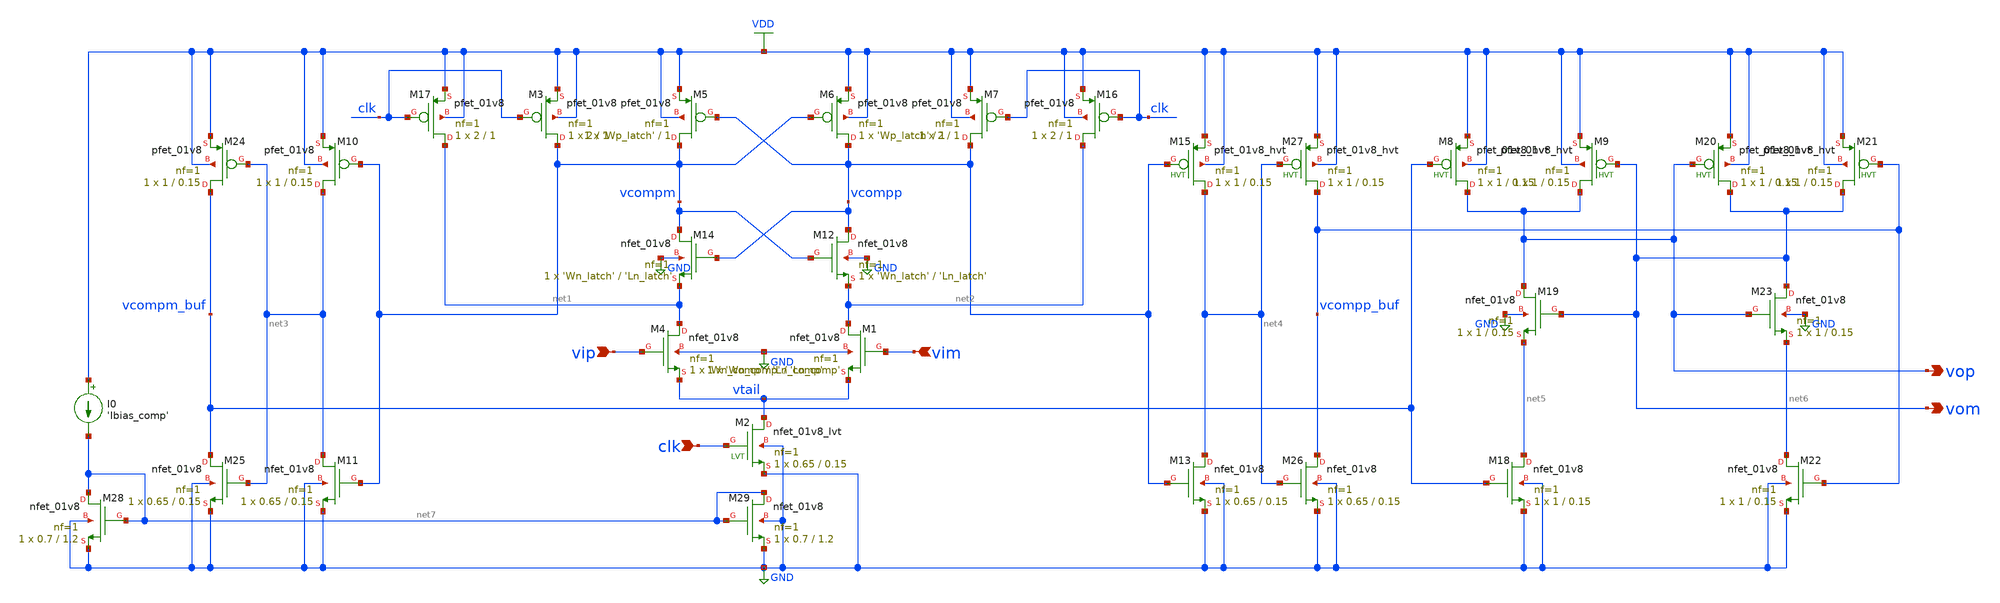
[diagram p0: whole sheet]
** sch_path: designs/latched_comparator.sch
* Copyright 2020 Stefan Frederik Schippers
* Licensed under the Apache License, Version 2.0 (the "License");
* you may not use this file except in compliance with the License.
* You may obtain a copy of the License at
* https://www.apache.org/licenses/LICENSE-2.0
* Unless required by applicable law or agreed to in writing, software
* distributed under the License is distributed on an "AS IS" BASIS,
* WITHOUT WARRANTIES OR CONDITIONS OF ANY KIND, either express or implied.
* See the License for the specific language governing permissions and
* limitations under the License.
**.subckt latched_comparator vip vim vop clk vom
*.ipin vip
*.ipin vim
*.opin vop
*.ipin clk
*.opin vom
XM5 vcompm vcompp VDD VDD sky130_fd_pr__pfet_01v8 L=1 W='Wp_latch' nf=1 ad='int((nf+1)/2) * W/nf * 0.29'
+ as='int((nf+2)/2) * W/nf * 0.29' pd='2*int((nf+1)/2) * (W/nf + 0.29)' ps='2*int((nf+2)/2) * (W/nf + 0.29)'
+ nrd='0.29 / W' nrs='0.29 / W' sa=0 sb=0 sd=0 mult=1 m=1
XM10 net3 vcompm VDD VDD sky130_fd_pr__pfet_01v8 L=0.15 W=1 nf=1 ad='int((nf+1)/2) * W/nf * 0.29' as='int((nf+2)/2) * W/nf * 0.29'
+ pd='2*int((nf+1)/2) * (W/nf + 0.29)' ps='2*int((nf+2)/2) * (W/nf + 0.29)' nrd='0.29 / W' nrs='0.29 / W'
+ sa=0 sb=0 sd=0 mult=1 m=1
XM11 net3 vcompm GND GND sky130_fd_pr__nfet_01v8 L=0.15 W=0.65 nf=1 ad='int((nf+1)/2) * W/nf * 0.29'
+ as='int((nf+2)/2) * W/nf * 0.29' pd='2*int((nf+1)/2) * (W/nf + 0.29)' ps='2*int((nf+2)/2) * (W/nf + 0.29)'
+ nrd='0.29 / W' nrs='0.29 / W' sa=0 sb=0 sd=0 mult=1 m=1
XM13 net4 vcompp GND GND sky130_fd_pr__nfet_01v8 L=0.15 W=0.65 nf=1 ad='int((nf+1)/2) * W/nf * 0.29'
+ as='int((nf+2)/2) * W/nf * 0.29' pd='2*int((nf+1)/2) * (W/nf + 0.29)' ps='2*int((nf+2)/2) * (W/nf + 0.29)'
+ nrd='0.29 / W' nrs='0.29 / W' sa=0 sb=0 sd=0 mult=1 m=1
XM15 net4 vcompp VDD VDD sky130_fd_pr__pfet_01v8_hvt L=0.15 W=1 nf=1 ad='int((nf+1)/2) * W/nf * 0.29'
+ as='int((nf+2)/2) * W/nf * 0.29' pd='2*int((nf+1)/2) * (W/nf + 0.29)' ps='2*int((nf+2)/2) * (W/nf + 0.29)'
+ nrd='0.29 / W' nrs='0.29 / W' sa=0 sb=0 sd=0 mult=1 m=1
XM6 vcompp vcompm VDD VDD sky130_fd_pr__pfet_01v8 L=1 W='Wp_latch' nf=1 ad='int((nf+1)/2) * W/nf * 0.29'
+ as='int((nf+2)/2) * W/nf * 0.29' pd='2*int((nf+1)/2) * (W/nf + 0.29)' ps='2*int((nf+2)/2) * (W/nf + 0.29)'
+ nrd='0.29 / W' nrs='0.29 / W' sa=0 sb=0 sd=0 mult=1 m=1
XM12 vcompp vcompm net2 GND sky130_fd_pr__nfet_01v8 L='Ln_latch' W='Wn_latch' nf=1 ad='int((nf+1)/2) * W/nf * 0.29'
+ as='int((nf+2)/2) * W/nf * 0.29' pd='2*int((nf+1)/2) * (W/nf + 0.29)' ps='2*int((nf+2)/2) * (W/nf + 0.29)'
+ nrd='0.29 / W' nrs='0.29 / W' sa=0 sb=0 sd=0 mult=1 m=1
XM14 vcompm vcompp net1 GND sky130_fd_pr__nfet_01v8 L='Ln_latch' W='Wn_latch' nf=1 ad='int((nf+1)/2) * W/nf * 0.29'
+ as='int((nf+2)/2) * W/nf * 0.29' pd='2*int((nf+1)/2) * (W/nf + 0.29)' ps='2*int((nf+2)/2) * (W/nf + 0.29)'
+ nrd='0.29 / W' nrs='0.29 / W' sa=0 sb=0 sd=0 mult=1 m=1
XM3 vcompm clk VDD VDD sky130_fd_pr__pfet_01v8 L=1 W=2 nf=1 ad='int((nf+1)/2) * W/nf * 0.29' as='int((nf+2)/2) * W/nf * 0.29'
+ pd='2*int((nf+1)/2) * (W/nf + 0.29)' ps='2*int((nf+2)/2) * (W/nf + 0.29)' nrd='0.29 / W' nrs='0.29 / W'
+ sa=0 sb=0 sd=0 mult=1 m=1
XM7 vcompp clk VDD VDD sky130_fd_pr__pfet_01v8 L=1 W=2 nf=1 ad='int((nf+1)/2) * W/nf * 0.29' as='int((nf+2)/2) * W/nf * 0.29'
+ pd='2*int((nf+1)/2) * (W/nf + 0.29)' ps='2*int((nf+2)/2) * (W/nf + 0.29)' nrd='0.29 / W' nrs='0.29 / W'
+ sa=0 sb=0 sd=0 mult=1 m=1
XM16 net2 clk VDD VDD sky130_fd_pr__pfet_01v8 L=1 W=2 nf=1 ad='int((nf+1)/2) * W/nf * 0.29' as='int((nf+2)/2) * W/nf * 0.29'
+ pd='2*int((nf+1)/2) * (W/nf + 0.29)' ps='2*int((nf+2)/2) * (W/nf + 0.29)' nrd='0.29 / W' nrs='0.29 / W'
+ sa=0 sb=0 sd=0 mult=1 m=1
XM17 net1 clk VDD VDD sky130_fd_pr__pfet_01v8 L=1 W=2 nf=1 ad='int((nf+1)/2) * W/nf * 0.29' as='int((nf+2)/2) * W/nf * 0.29'
+ pd='2*int((nf+1)/2) * (W/nf + 0.29)' ps='2*int((nf+2)/2) * (W/nf + 0.29)' nrd='0.29 / W' nrs='0.29 / W'
+ sa=0 sb=0 sd=0 mult=1 m=1
XM8 vop vcompm_buf VDD VDD sky130_fd_pr__pfet_01v8_hvt L=0.15 W=1 nf=1 ad='int((nf+1)/2) * W/nf * 0.29'
+ as='int((nf+2)/2) * W/nf * 0.29' pd='2*int((nf+1)/2) * (W/nf + 0.29)' ps='2*int((nf+2)/2) * (W/nf + 0.29)'
+ nrd='0.29 / W' nrs='0.29 / W' sa=0 sb=0 sd=0 mult=1 m=1
XM9 vop vom VDD VDD sky130_fd_pr__pfet_01v8_hvt L=0.15 W=1 nf=1 ad='int((nf+1)/2) * W/nf * 0.29' as='int((nf+2)/2) * W/nf * 0.29'
+ pd='2*int((nf+1)/2) * (W/nf + 0.29)' ps='2*int((nf+2)/2) * (W/nf + 0.29)' nrd='0.29 / W' nrs='0.29 / W'
+ sa=0 sb=0 sd=0 mult=1 m=1
XM18 net5 vcompm_buf GND GND sky130_fd_pr__nfet_01v8 L=0.15 W=1 nf=1 ad='int((nf+1)/2) * W/nf * 0.29'
+ as='int((nf+2)/2) * W/nf * 0.29' pd='2*int((nf+1)/2) * (W/nf + 0.29)' ps='2*int((nf+2)/2) * (W/nf + 0.29)'
+ nrd='0.29 / W' nrs='0.29 / W' sa=0 sb=0 sd=0 mult=1 m=1
XM19 vop vom net5 GND sky130_fd_pr__nfet_01v8 L=0.15 W=1 nf=1 ad='int((nf+1)/2) * W/nf * 0.29' as='int((nf+2)/2) * W/nf * 0.29'
+ pd='2*int((nf+1)/2) * (W/nf + 0.29)' ps='2*int((nf+2)/2) * (W/nf + 0.29)' nrd='0.29 / W' nrs='0.29 / W'
+ sa=0 sb=0 sd=0 mult=1 m=1
XM20 vom vop VDD VDD sky130_fd_pr__pfet_01v8_hvt L=0.15 W=1 nf=1 ad='int((nf+1)/2) * W/nf * 0.29' as='int((nf+2)/2) * W/nf * 0.29'
+ pd='2*int((nf+1)/2) * (W/nf + 0.29)' ps='2*int((nf+2)/2) * (W/nf + 0.29)' nrd='0.29 / W' nrs='0.29 / W'
+ sa=0 sb=0 sd=0 mult=1 m=1
XM21 vom vcompp_buf VDD VDD sky130_fd_pr__pfet_01v8_hvt L=0.15 W=1 nf=1 ad='int((nf+1)/2) * W/nf * 0.29'
+ as='int((nf+2)/2) * W/nf * 0.29' pd='2*int((nf+1)/2) * (W/nf + 0.29)' ps='2*int((nf+2)/2) * (W/nf + 0.29)'
+ nrd='0.29 / W' nrs='0.29 / W' sa=0 sb=0 sd=0 mult=1 m=1
XM22 net6 vcompp_buf GND GND sky130_fd_pr__nfet_01v8 L=0.15 W=1 nf=1 ad='int((nf+1)/2) * W/nf * 0.29'
+ as='int((nf+2)/2) * W/nf * 0.29' pd='2*int((nf+1)/2) * (W/nf + 0.29)' ps='2*int((nf+2)/2) * (W/nf + 0.29)'
+ nrd='0.29 / W' nrs='0.29 / W' sa=0 sb=0 sd=0 mult=1 m=1
XM23 vom vop net6 GND sky130_fd_pr__nfet_01v8 L=0.15 W=1 nf=1 ad='int((nf+1)/2) * W/nf * 0.29' as='int((nf+2)/2) * W/nf * 0.29'
+ pd='2*int((nf+1)/2) * (W/nf + 0.29)' ps='2*int((nf+2)/2) * (W/nf + 0.29)' nrd='0.29 / W' nrs='0.29 / W'
+ sa=0 sb=0 sd=0 mult=1 m=1
XM24 vcompm_buf net3 VDD VDD sky130_fd_pr__pfet_01v8 L=0.15 W=1 nf=1 ad='int((nf+1)/2) * W/nf * 0.29'
+ as='int((nf+2)/2) * W/nf * 0.29' pd='2*int((nf+1)/2) * (W/nf + 0.29)' ps='2*int((nf+2)/2) * (W/nf + 0.29)'
+ nrd='0.29 / W' nrs='0.29 / W' sa=0 sb=0 sd=0 mult=1 m=1
XM25 vcompm_buf net3 GND GND sky130_fd_pr__nfet_01v8 L=0.15 W=0.65 nf=1 ad='int((nf+1)/2) * W/nf * 0.29'
+ as='int((nf+2)/2) * W/nf * 0.29' pd='2*int((nf+1)/2) * (W/nf + 0.29)' ps='2*int((nf+2)/2) * (W/nf + 0.29)'
+ nrd='0.29 / W' nrs='0.29 / W' sa=0 sb=0 sd=0 mult=1 m=1
XM26 vcompp_buf net4 GND GND sky130_fd_pr__nfet_01v8 L=0.15 W=0.65 nf=1 ad='int((nf+1)/2) * W/nf * 0.29'
+ as='int((nf+2)/2) * W/nf * 0.29' pd='2*int((nf+1)/2) * (W/nf + 0.29)' ps='2*int((nf+2)/2) * (W/nf + 0.29)'
+ nrd='0.29 / W' nrs='0.29 / W' sa=0 sb=0 sd=0 mult=1 m=1
XM27 vcompp_buf net4 VDD VDD sky130_fd_pr__pfet_01v8_hvt L=0.15 W=1 nf=1 ad='int((nf+1)/2) * W/nf * 0.29'
+ as='int((nf+2)/2) * W/nf * 0.29' pd='2*int((nf+1)/2) * (W/nf + 0.29)' ps='2*int((nf+2)/2) * (W/nf + 0.29)'
+ nrd='0.29 / W' nrs='0.29 / W' sa=0 sb=0 sd=0 mult=1 m=1
I0 VDD net7 'Ibias_comp'
XM28 net7 net7 GND GND sky130_fd_pr__nfet_01v8 L=1.2 W=0.7 nf=1 ad='int((nf+1)/2) * W/nf * 0.29' as='int((nf+2)/2) * W/nf * 0.29'
+ pd='2*int((nf+1)/2) * (W/nf + 0.29)' ps='2*int((nf+2)/2) * (W/nf + 0.29)' nrd='0.29 / W' nrs='0.29 / W'
+ sa=0 sb=0 sd=0 mult=1 m=1
XM29 net7 net7 GND GND sky130_fd_pr__nfet_01v8 L=1.2 W=0.7 nf=1 ad='int((nf+1)/2) * W/nf * 0.29' as='int((nf+2)/2) * W/nf * 0.29'
+ pd='2*int((nf+1)/2) * (W/nf + 0.29)' ps='2*int((nf+2)/2) * (W/nf + 0.29)' nrd='0.29 / W' nrs='0.29 / W'
+ sa=0 sb=0 sd=0 mult=1 m=1
XM2 vtail clk GND GND sky130_fd_pr__nfet_01v8_lvt L=0.15 W=0.65 nf=1 ad='int((nf+1)/2) * W/nf * 0.29'
+ as='int((nf+2)/2) * W/nf * 0.29' pd='2*int((nf+1)/2) * (W/nf + 0.29)' ps='2*int((nf+2)/2) * (W/nf + 0.29)'
+ nrd='0.29 / W' nrs='0.29 / W' sa=0 sb=0 sd=0 mult=1 m=1
XM1 net2 vim vtail GND sky130_fd_pr__nfet_01v8 L='Ln_comp' W='Wn_comp' nf=1 ad='int((nf+1)/2) * W/nf * 0.29'
+ as='int((nf+2)/2) * W/nf * 0.29' pd='2*int((nf+1)/2) * (W/nf + 0.29)' ps='2*int((nf+2)/2) * (W/nf + 0.29)'
+ nrd='0.29 / W' nrs='0.29 / W' sa=0 sb=0 sd=0 mult=1 m=1
XM4 net1 vip vtail GND sky130_fd_pr__nfet_01v8 L='Ln_comp' W='Wn_comp' nf=1 ad='int((nf+1)/2) * W/nf * 0.29'
+ as='int((nf+2)/2) * W/nf * 0.29' pd='2*int((nf+1)/2) * (W/nf + 0.29)' ps='2*int((nf+2)/2) * (W/nf + 0.29)'
+ nrd='0.29 / W' nrs='0.29 / W' sa=0 sb=0 sd=0 mult=1 m=1
**** begin user architecture code

.include $::SKYWATER_MODELS/cells/nfet_01v8/sky130_fd_pr__nfet_01v8__tt.corner.spice
.include $::SKYWATER_MODELS/cells/nfet_01v8_lvt/sky130_fd_pr__nfet_01v8_lvt__tt.corner.spice
.include $::SKYWATER_MODELS/cells/pfet_01v8/sky130_fd_pr__pfet_01v8__tt.corner.spice
.include $::SKYWATER_MODELS/cells/nfet_03v3_nvt/sky130_fd_pr__nfet_03v3_nvt__tt.corner.spice
.include $::SKYWATER_MODELS/cells/nfet_05v0_nvt/sky130_fd_pr__nfet_05v0_nvt__tt.corner.spice
.include $::SKYWATER_MODELS/cells/esd_nfet_01v8/sky130_fd_pr__esd_nfet_01v8__tt.corner.spice
.include $::SKYWATER_MODELS/cells/pfet_01v8_lvt/sky130_fd_pr__pfet_01v8_lvt__tt.corner.spice
.include $::SKYWATER_MODELS/cells/pfet_01v8_hvt/sky130_fd_pr__pfet_01v8_hvt__tt.corner.spice
.include $::SKYWATER_MODELS/cells/esd_pfet_g5v0d10v5/sky130_fd_pr__esd_pfet_g5v0d10v5__tt.corner.spice
.include $::SKYWATER_MODELS/cells/pfet_g5v0d10v5/sky130_fd_pr__pfet_g5v0d10v5__tt.corner.spice
.include $::SKYWATER_MODELS/cells/pfet_g5v0d16v0/sky130_fd_pr__pfet_g5v0d16v0__tt.corner.spice
.include $::SKYWATER_MODELS/cells/nfet_g5v0d10v5/sky130_fd_pr__nfet_g5v0d10v5__tt.corner.spice
.include $::SKYWATER_MODELS/cells/nfet_g5v0d16v0/sky130_fd_pr__nfet_g5v0d16v0__tt_discrete.corner.spice
.include $::SKYWATER_MODELS/cells/esd_nfet_g5v0d10v5/sky130_fd_pr__esd_nfet_g5v0d10v5__tt.corner.spice
.include $::SKYWATER_MODELS/models/corners/tt/nonfet.spice
* Mismatch parameters
.include $::SKYWATER_MODELS/cells/nfet_01v8/sky130_fd_pr__nfet_01v8__mismatch.corner.spice
.include $::SKYWATER_MODELS/cells/pfet_01v8/sky130_fd_pr__pfet_01v8__mismatch.corner.spice
.include $::SKYWATER_MODELS/cells/nfet_01v8_lvt/sky130_fd_pr__nfet_01v8_lvt__mismatch.corner.spice
.include $::SKYWATER_MODELS/cells/pfet_01v8_lvt/sky130_fd_pr__pfet_01v8_lvt__mismatch.corner.spice
.include $::SKYWATER_MODELS/cells/pfet_01v8_hvt/sky130_fd_pr__pfet_01v8_hvt__mismatch.corner.spice
.include $::SKYWATER_MODELS/cells/nfet_g5v0d10v5/sky130_fd_pr__nfet_g5v0d10v5__mismatch.corner.spice
.include $::SKYWATER_MODELS/cells/pfet_g5v0d10v5/sky130_fd_pr__pfet_g5v0d10v5__mismatch.corner.spice
.include $::SKYWATER_MODELS/cells/nfet_05v0_nvt/sky130_fd_pr__nfet_05v0_nvt__mismatch.corner.spice
.include $::SKYWATER_MODELS/cells/nfet_03v3_nvt/sky130_fd_pr__nfet_03v3_nvt__mismatch.corner.spice
* Resistor$::SKYWATER_MODELS/Capacitor
.include $::SKYWATER_MODELS/models/r+c/res_typical__cap_typical.spice
.include $::SKYWATER_MODELS/models/r+c/res_typical__cap_typical__lin.spice
* Special cells
.include $::SKYWATER_MODELS/models/corners/tt/specialized_cells.spice
* All models
.include $::SKYWATER_MODELS/models/all.spice
* Corner
.include $::SKYWATER_MODELS/models/corners/tt/rf.spice

**** end user architecture code
**.ends
.GLOBAL VDD
.GLOBAL GND
**** begin user architecture code

.include latched_comparator_commands.spice

**** end user architecture code
.end
